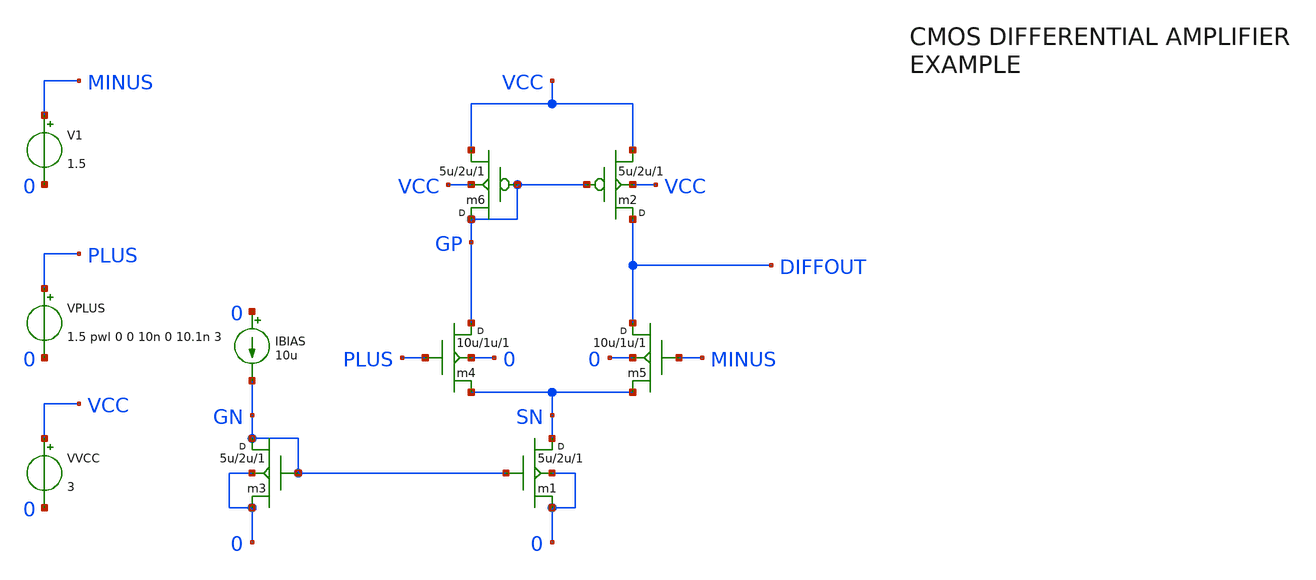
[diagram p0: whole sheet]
** sch_path: xschem_library/examples/cmos_example.sch
**.subckt cmos_example
m1 SN GN 0 0 cmosn w=5u l=2u m=1
m2 DIFFOUT GP VCC VCC cmosp w=5u l=2u m=1
VVCC VCC 0 3
m3 GN GN 0 0 cmosn w=5u l=2u m=1
IBIAS 0 GN 10u
m4 GP PLUS SN 0 cmosn w=10u l=1u m=1
m5 DIFFOUT MINUS SN 0 cmosn w=10u l=1u m=1
m6 GP GP VCC VCC cmosp w=5u l=2u m=1
VPLUS PLUS 0 1.5 pwl 0 0 10n 0 10.1n 3
V1 MINUS 0 1.5
**** begin user architecture code

.option PARHIER=LOCAL RUNLVL=6 post MODMONTE=1 warn maxwarns=400
.option sampling_method = SRS
.option method=gear
.temp 30

.save all
** models are generally not free: you must download
** SPICE models for active devices and put them  into the below
** referenced file in netlist/simulation directory.
.include "models_cmos_example.txt"
* .dc VPLUS 1.3 1.7 0.001
.tran 0.02n 20n
.probe i(*)


**** end user architecture code
**.ends
.end
